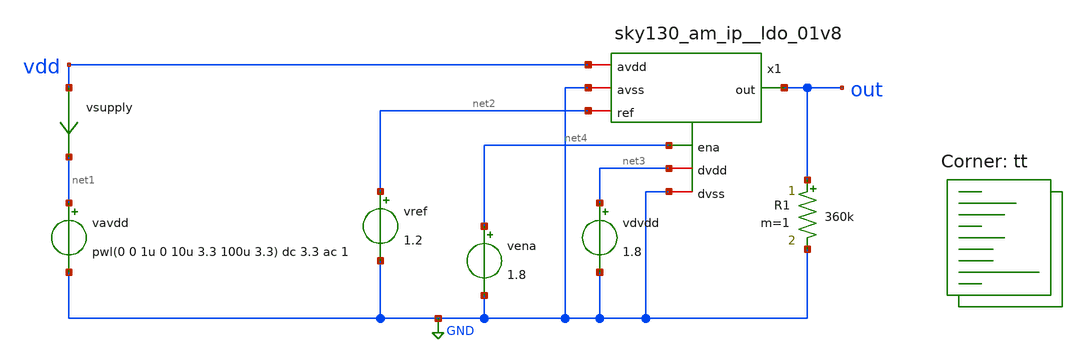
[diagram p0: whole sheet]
** sch_path: xschem/sky130_am_ip__ldo_01v8_tb.sch
**.subckt sky130_am_ip__ldo_01v8_tb
vavdd net1 GND pwl(0 0 1u 0 10u 3.3 100u 3.3) dc 3.3 ac 1
vsupply vdd net1 0
.save i(vsupply)
x1 vdd net3 net4 out GND GND net2 sky130_am_ip__ldo_01v8
R1 out GND 360k m=1
vref net2 GND 1.2
vdvdd net3 GND 1.8
vena net4 GND 1.8
**** begin user architecture code

.option savecurrents
.control
save all
op
write sky130_am_ip__ldo_01v8_tb.raw
set appendwrite

ac dec 10 10 1e9
set units=degrees
plot db(out)

dc vavdd 0 3.3 10m
plot v(out)

tran 100n 100u
plot v(out)
.endc


.lib $::SKYWATER_MODELS/sky130.lib.spice tt
**** end user architecture code
**.ends

* expanding   symbol:  sky130_am_ip__ldo_01v8.sym # of pins=7
** sym_path: xschem/sky130_am_ip__ldo_01v8.sym
** sch_path: xschem/sky130_am_ip__ldo_01v8.sch
.subckt sky130_am_ip__ldo_01v8 avdd dvdd ena out avss dvss ref
*.opin out
*.iopin dvdd
*.iopin dvss
*.ipin ref
*.ipin ena
*.iopin avdd
*.iopin avss
XM11 avdd v_ea out avss sky130_fd_pr__nfet_g5v0d10v5 L=1 W=200 nf=1 ad='int((nf+1)/2) * W/nf * 0.29'
+ as='int((nf+2)/2) * W/nf * 0.29' pd='2*int((nf+1)/2) * (W/nf + 0.29)' ps='2*int((nf+2)/2) * (W/nf + 0.29)'
+ nrd='0.29 / W' nrs='0.29 / W' sa=0 sb=0 sd=0 mult=1 m=1
XR1 v_m out avss sky130_fd_pr__res_high_po_0p35 L=1000 mult=1 m=1
XR2 avss v_m avss sky130_fd_pr__res_high_po_0p35 L=2000 mult=1 m=1
XM10 vi vi avdd avdd sky130_fd_pr__pfet_g5v0d10v5 L=20 W=1 nf=1 ad='int((nf+1)/2) * W/nf * 0.29' as='int((nf+2)/2) * W/nf * 0.29'
+ pd='2*int((nf+1)/2) * (W/nf + 0.29)' ps='2*int((nf+2)/2) * (W/nf + 0.29)' nrd='0.29 / W' nrs='0.29 / W'
+ sa=0 sb=0 sd=0 mult=1 m=1
XM16 vi vi avss avss sky130_fd_pr__nfet_g5v0d10v5 L=20 W=2.5 nf=1 ad='int((nf+1)/2) * W/nf * 0.29' as='int((nf+2)/2) * W/nf * 0.29'
+ pd='2*int((nf+1)/2) * (W/nf + 0.29)' ps='2*int((nf+2)/2) * (W/nf + 0.29)' nrd='0.29 / W' nrs='0.29 / W'
+ sa=0 sb=0 sd=0 mult=1 m=1
x1 ena dvdd v_ea v_m ref dvss avdd avss error_amplifier
.ends


* expanding   symbol:  error_amplifier.sym # of pins=8
** sym_path: xschem/error_amplifier.sym
** sch_path: xschem/error_amplifier.sch
.subckt error_amplifier ena dvdd out in_m in_p dvss avdd avss
*.iopin avdd
*.iopin avss
*.ipin in_m
*.ipin in_p
*.opin out
*.ipin ena
*.iopin dvdd
*.iopin dvss
XM1 vbn vbn avss avss sky130_fd_pr__nfet_g5v0d10v5 L=10 W=1 nf=1 ad='int((nf+1)/2) * W/nf * 0.29' as='int((nf+2)/2) * W/nf * 0.29'
+ pd='2*int((nf+1)/2) * (W/nf + 0.29)' ps='2*int((nf+2)/2) * (W/nf + 0.29)' nrd='0.29 / W' nrs='0.29 / W'
+ sa=0 sb=0 sd=0 mult=1 m=1
XM3 vcp vbn net6 avss sky130_fd_pr__nfet_g5v0d10v5 L=10 W=1 nf=1 ad='int((nf+1)/2) * W/nf * 0.29' as='int((nf+2)/2) * W/nf * 0.29'
+ pd='2*int((nf+1)/2) * (W/nf + 0.29)' ps='2*int((nf+2)/2) * (W/nf + 0.29)' nrd='0.29 / W' nrs='0.29 / W'
+ sa=0 sb=0 sd=0 mult=4 m=4
XM5 vbp vbp avdd avdd sky130_fd_pr__pfet_g5v0d10v5 L=10 W=1 nf=1 ad='int((nf+1)/2) * W/nf * 0.29' as='int((nf+2)/2) * W/nf * 0.29'
+ pd='2*int((nf+1)/2) * (W/nf + 0.29)' ps='2*int((nf+2)/2) * (W/nf + 0.29)' nrd='0.29 / W' nrs='0.29 / W'
+ sa=0 sb=0 sd=0 mult=2 m=2
XM26 net4 vbp avdd avdd sky130_fd_pr__pfet_g5v0d10v5 L=10 W=1 nf=1 ad='int((nf+1)/2) * W/nf * 0.29' as='int((nf+2)/2) * W/nf * 0.29'
+ pd='2*int((nf+1)/2) * (W/nf + 0.29)' ps='2*int((nf+2)/2) * (W/nf + 0.29)' nrd='0.29 / W' nrs='0.29 / W'
+ sa=0 sb=0 sd=0 mult=6 m=6
XM27 net5 vbp avdd avdd sky130_fd_pr__pfet_g5v0d10v5 L=10 W=1 nf=1 ad='int((nf+1)/2) * W/nf * 0.29' as='int((nf+2)/2) * W/nf * 0.29'
+ pd='2*int((nf+1)/2) * (W/nf + 0.29)' ps='2*int((nf+2)/2) * (W/nf + 0.29)' nrd='0.29 / W' nrs='0.29 / W'
+ sa=0 sb=0 sd=0 mult=6 m=6
XM28 net3 vcp net4 avdd sky130_fd_pr__pfet_g5v0d10v5 L=2 W=1 nf=1 ad='int((nf+1)/2) * W/nf * 0.29' as='int((nf+2)/2) * W/nf * 0.29'
+ pd='2*int((nf+1)/2) * (W/nf + 0.29)' ps='2*int((nf+2)/2) * (W/nf + 0.29)' nrd='0.29 / W' nrs='0.29 / W'
+ sa=0 sb=0 sd=0 mult=1 m=1
XM29 v_cascode vcp net5 avdd sky130_fd_pr__pfet_g5v0d10v5 L=2 W=1 nf=1 ad='int((nf+1)/2) * W/nf * 0.29'
+ as='int((nf+2)/2) * W/nf * 0.29' pd='2*int((nf+1)/2) * (W/nf + 0.29)' ps='2*int((nf+2)/2) * (W/nf + 0.29)'
+ nrd='0.29 / W' nrs='0.29 / W' sa=0 sb=0 sd=0 mult=1 m=1
XM30 net3 vcn net1 avss sky130_fd_pr__nfet_g5v0d10v5 L=2 W=1 nf=1 ad='int((nf+1)/2) * W/nf * 0.29' as='int((nf+2)/2) * W/nf * 0.29'
+ pd='2*int((nf+1)/2) * (W/nf + 0.29)' ps='2*int((nf+2)/2) * (W/nf + 0.29)' nrd='0.29 / W' nrs='0.29 / W'
+ sa=0 sb=0 sd=0 mult=1 m=1
XM31 v_cascode vcn net2 avss sky130_fd_pr__nfet_g5v0d10v5 L=2 W=1 nf=1 ad='int((nf+1)/2) * W/nf * 0.29'
+ as='int((nf+2)/2) * W/nf * 0.29' pd='2*int((nf+1)/2) * (W/nf + 0.29)' ps='2*int((nf+2)/2) * (W/nf + 0.29)'
+ nrd='0.29 / W' nrs='0.29 / W' sa=0 sb=0 sd=0 mult=1 m=1
XM32 net1 net3 avss avss sky130_fd_pr__nfet_g5v0d10v5 L=10 W=1 nf=1 ad='int((nf+1)/2) * W/nf * 0.29'
+ as='int((nf+2)/2) * W/nf * 0.29' pd='2*int((nf+1)/2) * (W/nf + 0.29)' ps='2*int((nf+2)/2) * (W/nf + 0.29)'
+ nrd='0.29 / W' nrs='0.29 / W' sa=0 sb=0 sd=0 mult=3 m=3
XM33 net2 net3 avss avss sky130_fd_pr__nfet_g5v0d10v5 L=10 W=1 nf=1 ad='int((nf+1)/2) * W/nf * 0.29'
+ as='int((nf+2)/2) * W/nf * 0.29' pd='2*int((nf+1)/2) * (W/nf + 0.29)' ps='2*int((nf+2)/2) * (W/nf + 0.29)'
+ nrd='0.29 / W' nrs='0.29 / W' sa=0 sb=0 sd=0 mult=3 m=3
XM35 net11 vbp avdd avdd sky130_fd_pr__pfet_g5v0d10v5 L=10 W=1 nf=1 ad='int((nf+1)/2) * W/nf * 0.29'
+ as='int((nf+2)/2) * W/nf * 0.29' pd='2*int((nf+1)/2) * (W/nf + 0.29)' ps='2*int((nf+2)/2) * (W/nf + 0.29)'
+ nrd='0.29 / W' nrs='0.29 / W' sa=0 sb=0 sd=0 mult=2 m=2
XR3 avss net6 avss sky130_fd_pr__res_xhigh_po_0p35 L=180 mult=1 m=1
XM9 net13 v_cascode out avdd sky130_fd_pr__pfet_g5v0d10v5 L=10 W=1 nf=1 ad='int((nf+1)/2) * W/nf * 0.29'
+ as='int((nf+2)/2) * W/nf * 0.29' pd='2*int((nf+1)/2) * (W/nf + 0.29)' ps='2*int((nf+2)/2) * (W/nf + 0.29)'
+ nrd='0.29 / W' nrs='0.29 / W' sa=0 sb=0 sd=0 mult=1 m=1
XM8 out vbp avdd avdd sky130_fd_pr__pfet_g5v0d10v5 L=10 W=1 nf=1 ad='int((nf+1)/2) * W/nf * 0.29' as='int((nf+2)/2) * W/nf * 0.29'
+ pd='2*int((nf+1)/2) * (W/nf + 0.29)' ps='2*int((nf+2)/2) * (W/nf + 0.29)' nrd='0.29 / W' nrs='0.29 / W'
+ sa=0 sb=0 sd=0 mult=10 m=10
XM17 net8 vbp avdd avdd sky130_fd_pr__pfet_g5v0d10v5 L=10 W=1 nf=1 ad='int((nf+1)/2) * W/nf * 0.29' as='int((nf+2)/2) * W/nf * 0.29'
+ pd='2*int((nf+1)/2) * (W/nf + 0.29)' ps='2*int((nf+2)/2) * (W/nf + 0.29)' nrd='0.29 / W' nrs='0.29 / W'
+ sa=0 sb=0 sd=0 mult=1 m=1
XM19 net8 net8 net7 avss sky130_fd_pr__nfet_g5v0d10v5 L=0.5 W=1 nf=1 ad='int((nf+1)/2) * W/nf * 0.29'
+ as='int((nf+2)/2) * W/nf * 0.29' pd='2*int((nf+1)/2) * (W/nf + 0.29)' ps='2*int((nf+2)/2) * (W/nf + 0.29)'
+ nrd='0.29 / W' nrs='0.29 / W' sa=0 sb=0 sd=0 mult=6 m=6
XM20 net7 net8 avss avss sky130_fd_pr__nfet_g5v0d10v5 L=0.5 W=1 nf=1 ad='int((nf+1)/2) * W/nf * 0.29'
+ as='int((nf+2)/2) * W/nf * 0.29' pd='2*int((nf+1)/2) * (W/nf + 0.29)' ps='2*int((nf+2)/2) * (W/nf + 0.29)'
+ nrd='0.29 / W' nrs='0.29 / W' sa=0 sb=0 sd=0 mult=1 m=1
XM21 vcn vbp avdd avdd sky130_fd_pr__pfet_g5v0d10v5 L=10 W=1 nf=1 ad='int((nf+1)/2) * W/nf * 0.29' as='int((nf+2)/2) * W/nf * 0.29'
+ pd='2*int((nf+1)/2) * (W/nf + 0.29)' ps='2*int((nf+2)/2) * (W/nf + 0.29)' nrd='0.29 / W' nrs='0.29 / W'
+ sa=0 sb=0 sd=0 mult=5 m=5
XM36 vcn vcn net7 avss sky130_fd_pr__nfet_g5v0d10v5 L=2 W=1 nf=1 ad='int((nf+1)/2) * W/nf * 0.29' as='int((nf+2)/2) * W/nf * 0.29'
+ pd='2*int((nf+1)/2) * (W/nf + 0.29)' ps='2*int((nf+2)/2) * (W/nf + 0.29)' nrd='0.29 / W' nrs='0.29 / W'
+ sa=0 sb=0 sd=0 mult=1 m=1
XM6 net5 in_m net9 avss sky130_fd_pr__nfet_g5v0d10v5 L=0.5 W=1 nf=1 ad='int((nf+1)/2) * W/nf * 0.29'
+ as='int((nf+2)/2) * W/nf * 0.29' pd='2*int((nf+1)/2) * (W/nf + 0.29)' ps='2*int((nf+2)/2) * (W/nf + 0.29)'
+ nrd='0.29 / W' nrs='0.29 / W' sa=0 sb=0 sd=0 mult=1 m=1
XM7 net9 vbn avss avss sky130_fd_pr__nfet_g5v0d10v5 L=10 W=1 nf=1 ad='int((nf+1)/2) * W/nf * 0.29' as='int((nf+2)/2) * W/nf * 0.29'
+ pd='2*int((nf+1)/2) * (W/nf + 0.29)' ps='2*int((nf+2)/2) * (W/nf + 0.29)' nrd='0.29 / W' nrs='0.29 / W'
+ sa=0 sb=0 sd=0 mult=2 m=2
XM12 net4 in_p net9 avss sky130_fd_pr__nfet_g5v0d10v5 L=0.5 W=1 nf=1 ad='int((nf+1)/2) * W/nf * 0.29'
+ as='int((nf+2)/2) * W/nf * 0.29' pd='2*int((nf+1)/2) * (W/nf + 0.29)' ps='2*int((nf+2)/2) * (W/nf + 0.29)'
+ nrd='0.29 / W' nrs='0.29 / W' sa=0 sb=0 sd=0 mult=1 m=1
XM10 vstart vbn avss avss sky130_fd_pr__nfet_g5v0d10v5 L=1 W=10 nf=1 ad='int((nf+1)/2) * W/nf * 0.29'
+ as='int((nf+2)/2) * W/nf * 0.29' pd='2*int((nf+1)/2) * (W/nf + 0.29)' ps='2*int((nf+2)/2) * (W/nf + 0.29)'
+ nrd='0.29 / W' nrs='0.29 / W' sa=0 sb=0 sd=0 mult=1 m=1
XM11 vstart avss net10 avdd sky130_fd_pr__pfet_g5v0d10v5 L=20 W=1 nf=1 ad='int((nf+1)/2) * W/nf * 0.29'
+ as='int((nf+2)/2) * W/nf * 0.29' pd='2*int((nf+1)/2) * (W/nf + 0.29)' ps='2*int((nf+2)/2) * (W/nf + 0.29)'
+ nrd='0.29 / W' nrs='0.29 / W' sa=0 sb=0 sd=0 mult=1 m=1
XM2 vcp vcp vbp avdd sky130_fd_pr__pfet_g5v0d10v5 L=10 W=1 nf=1 ad='int((nf+1)/2) * W/nf * 0.29' as='int((nf+2)/2) * W/nf * 0.29'
+ pd='2*int((nf+1)/2) * (W/nf + 0.29)' ps='2*int((nf+2)/2) * (W/nf + 0.29)' nrd='0.29 / W' nrs='0.29 / W'
+ sa=0 sb=0 sd=0 mult=2 m=2
XM4 vbn vcp net11 avdd sky130_fd_pr__pfet_g5v0d10v5 L=10 W=1 nf=1 ad='int((nf+1)/2) * W/nf * 0.29' as='int((nf+2)/2) * W/nf * 0.29'
+ pd='2*int((nf+1)/2) * (W/nf + 0.29)' ps='2*int((nf+2)/2) * (W/nf + 0.29)' nrd='0.29 / W' nrs='0.29 / W'
+ sa=0 sb=0 sd=0 mult=2 m=2
XM13 vbp vstart avss avss sky130_fd_pr__nfet_g5v0d10v5 L=0.5 W=1 nf=1 ad='int((nf+1)/2) * W/nf * 0.29'
+ as='int((nf+2)/2) * W/nf * 0.29' pd='2*int((nf+1)/2) * (W/nf + 0.29)' ps='2*int((nf+2)/2) * (W/nf + 0.29)'
+ nrd='0.29 / W' nrs='0.29 / W' sa=0 sb=0 sd=0 mult=1 m=1
XM14 vcp vstart avss avss sky130_fd_pr__nfet_g5v0d10v5 L=0.5 W=1 nf=1 ad='int((nf+1)/2) * W/nf * 0.29'
+ as='int((nf+2)/2) * W/nf * 0.29' pd='2*int((nf+1)/2) * (W/nf + 0.29)' ps='2*int((nf+2)/2) * (W/nf + 0.29)'
+ nrd='0.29 / W' nrs='0.29 / W' sa=0 sb=0 sd=0 mult=1 m=1
XM15 net10 net10 net12 avdd sky130_fd_pr__pfet_g5v0d10v5 L=20 W=1 nf=1 ad='int((nf+1)/2) * W/nf * 0.29'
+ as='int((nf+2)/2) * W/nf * 0.29' pd='2*int((nf+1)/2) * (W/nf + 0.29)' ps='2*int((nf+2)/2) * (W/nf + 0.29)'
+ nrd='0.29 / W' nrs='0.29 / W' sa=0 sb=0 sd=0 mult=1 m=1
XM16 vbp v_ena avdd avdd sky130_fd_pr__pfet_g5v0d10v5 L=0.5 W=1 nf=1 ad='int((nf+1)/2) * W/nf * 0.29'
+ as='int((nf+2)/2) * W/nf * 0.29' pd='2*int((nf+1)/2) * (W/nf + 0.29)' ps='2*int((nf+2)/2) * (W/nf + 0.29)'
+ nrd='0.29 / W' nrs='0.29 / W' sa=0 sb=0 sd=0 mult=1 m=1
XM18 vcp v_ena avdd avdd sky130_fd_pr__pfet_g5v0d10v5 L=0.5 W=1 nf=1 ad='int((nf+1)/2) * W/nf * 0.29'
+ as='int((nf+2)/2) * W/nf * 0.29' pd='2*int((nf+1)/2) * (W/nf + 0.29)' ps='2*int((nf+2)/2) * (W/nf + 0.29)'
+ nrd='0.29 / W' nrs='0.29 / W' sa=0 sb=0 sd=0 mult=1 m=1
XM22 vbn v_ena_b avss avss sky130_fd_pr__nfet_g5v0d10v5 L=0.5 W=1 nf=1 ad='int((nf+1)/2) * W/nf * 0.29'
+ as='int((nf+2)/2) * W/nf * 0.29' pd='2*int((nf+1)/2) * (W/nf + 0.29)' ps='2*int((nf+2)/2) * (W/nf + 0.29)'
+ nrd='0.29 / W' nrs='0.29 / W' sa=0 sb=0 sd=0 mult=1 m=1
XM23 vcn v_ena_b avss avss sky130_fd_pr__nfet_g5v0d10v5 L=0.5 W=1 nf=1 ad='int((nf+1)/2) * W/nf * 0.29'
+ as='int((nf+2)/2) * W/nf * 0.29' pd='2*int((nf+1)/2) * (W/nf + 0.29)' ps='2*int((nf+2)/2) * (W/nf + 0.29)'
+ nrd='0.29 / W' nrs='0.29 / W' sa=0 sb=0 sd=0 mult=1 m=1
XM24 v_cascode v_ena_b avss avss sky130_fd_pr__nfet_g5v0d10v5 L=0.5 W=1 nf=1 ad='int((nf+1)/2) * W/nf * 0.29'
+ as='int((nf+2)/2) * W/nf * 0.29' pd='2*int((nf+1)/2) * (W/nf + 0.29)' ps='2*int((nf+2)/2) * (W/nf + 0.29)'
+ nrd='0.29 / W' nrs='0.29 / W' sa=0 sb=0 sd=0 mult=1 m=1
XM25 out v_ena_b avss avss sky130_fd_pr__nfet_g5v0d10v5 L=0.5 W=1 nf=1 ad='int((nf+1)/2) * W/nf * 0.29'
+ as='int((nf+2)/2) * W/nf * 0.29' pd='2*int((nf+1)/2) * (W/nf + 0.29)' ps='2*int((nf+2)/2) * (W/nf + 0.29)'
+ nrd='0.29 / W' nrs='0.29 / W' sa=0 sb=0 sd=0 mult=1 m=1
XM34 vstart v_ena_b avss avss sky130_fd_pr__nfet_g5v0d10v5 L=0.5 W=1 nf=1 ad='int((nf+1)/2) * W/nf * 0.29'
+ as='int((nf+2)/2) * W/nf * 0.29' pd='2*int((nf+1)/2) * (W/nf + 0.29)' ps='2*int((nf+2)/2) * (W/nf + 0.29)'
+ nrd='0.29 / W' nrs='0.29 / W' sa=0 sb=0 sd=0 mult=1 m=1
XM37 net12 v_ena_b avdd avdd sky130_fd_pr__pfet_g5v0d10v5 L=0.5 W=1 nf=1 ad='int((nf+1)/2) * W/nf * 0.29'
+ as='int((nf+2)/2) * W/nf * 0.29' pd='2*int((nf+1)/2) * (W/nf + 0.29)' ps='2*int((nf+2)/2) * (W/nf + 0.29)'
+ nrd='0.29 / W' nrs='0.29 / W' sa=0 sb=0 sd=0 mult=1 m=1
XM38 net13 vbn avss avss sky130_fd_pr__nfet_g5v0d10v5 L=10 W=1 nf=1 ad='int((nf+1)/2) * W/nf * 0.29'
+ as='int((nf+2)/2) * W/nf * 0.29' pd='2*int((nf+1)/2) * (W/nf + 0.29)' ps='2*int((nf+2)/2) * (W/nf + 0.29)'
+ nrd='0.29 / W' nrs='0.29 / W' sa=0 sb=0 sd=0 mult=2 m=2
XM39 out net13 avss avss sky130_fd_pr__nfet_g5v0d10v5 L=0.5 W=4 nf=1 ad='int((nf+1)/2) * W/nf * 0.29'
+ as='int((nf+2)/2) * W/nf * 0.29' pd='2*int((nf+1)/2) * (W/nf + 0.29)' ps='2*int((nf+2)/2) * (W/nf + 0.29)'
+ nrd='0.29 / W' nrs='0.29 / W' sa=0 sb=0 sd=0 mult=1 m=1
XM41 ena_b ena dvdd dvdd sky130_fd_pr__pfet_g5v0d10v5 L=0.5 W=2.5 nf=1 ad='int((nf+1)/2) * W/nf * 0.29'
+ as='int((nf+2)/2) * W/nf * 0.29' pd='2*int((nf+1)/2) * (W/nf + 0.29)' ps='2*int((nf+2)/2) * (W/nf + 0.29)'
+ nrd='0.29 / W' nrs='0.29 / W' sa=0 sb=0 sd=0 mult=1 m=1
XM42 ena_b ena dvss dvss sky130_fd_pr__nfet_g5v0d10v5 L=0.5 W=1 nf=1 ad='int((nf+1)/2) * W/nf * 0.29'
+ as='int((nf+2)/2) * W/nf * 0.29' pd='2*int((nf+1)/2) * (W/nf + 0.29)' ps='2*int((nf+2)/2) * (W/nf + 0.29)'
+ nrd='0.29 / W' nrs='0.29 / W' sa=0 sb=0 sd=0 mult=1 m=1
XM43 v_ena v_ena_b avdd avdd sky130_fd_pr__pfet_g5v0d10v5 L=0.5 W=2.5 nf=1 ad='int((nf+1)/2) * W/nf * 0.29'
+ as='int((nf+2)/2) * W/nf * 0.29' pd='2*int((nf+1)/2) * (W/nf + 0.29)' ps='2*int((nf+2)/2) * (W/nf + 0.29)'
+ nrd='0.29 / W' nrs='0.29 / W' sa=0 sb=0 sd=0 mult=1 m=1
XM44 v_ena ena_b avss avss sky130_fd_pr__nfet_g5v0d10v5 L=0.5 W=1 nf=1 ad='int((nf+1)/2) * W/nf * 0.29'
+ as='int((nf+2)/2) * W/nf * 0.29' pd='2*int((nf+1)/2) * (W/nf + 0.29)' ps='2*int((nf+2)/2) * (W/nf + 0.29)'
+ nrd='0.29 / W' nrs='0.29 / W' sa=0 sb=0 sd=0 mult=1 m=1
XM45 v_ena_b v_ena avdd avdd sky130_fd_pr__pfet_g5v0d10v5 L=0.5 W=2.5 nf=1 ad='int((nf+1)/2) * W/nf * 0.29'
+ as='int((nf+2)/2) * W/nf * 0.29' pd='2*int((nf+1)/2) * (W/nf + 0.29)' ps='2*int((nf+2)/2) * (W/nf + 0.29)'
+ nrd='0.29 / W' nrs='0.29 / W' sa=0 sb=0 sd=0 mult=1 m=1
XM46 v_ena_b ena avss avss sky130_fd_pr__nfet_g5v0d10v5 L=0.5 W=1 nf=1 ad='int((nf+1)/2) * W/nf * 0.29'
+ as='int((nf+2)/2) * W/nf * 0.29' pd='2*int((nf+1)/2) * (W/nf + 0.29)' ps='2*int((nf+2)/2) * (W/nf + 0.29)'
+ nrd='0.29 / W' nrs='0.29 / W' sa=0 sb=0 sd=0 mult=1 m=1
XC1 out v_cascode sky130_fd_pr__cap_mim_m3_1 W=6 L=6 MF=4 m=4
.ends

.GLOBAL GND
.end
